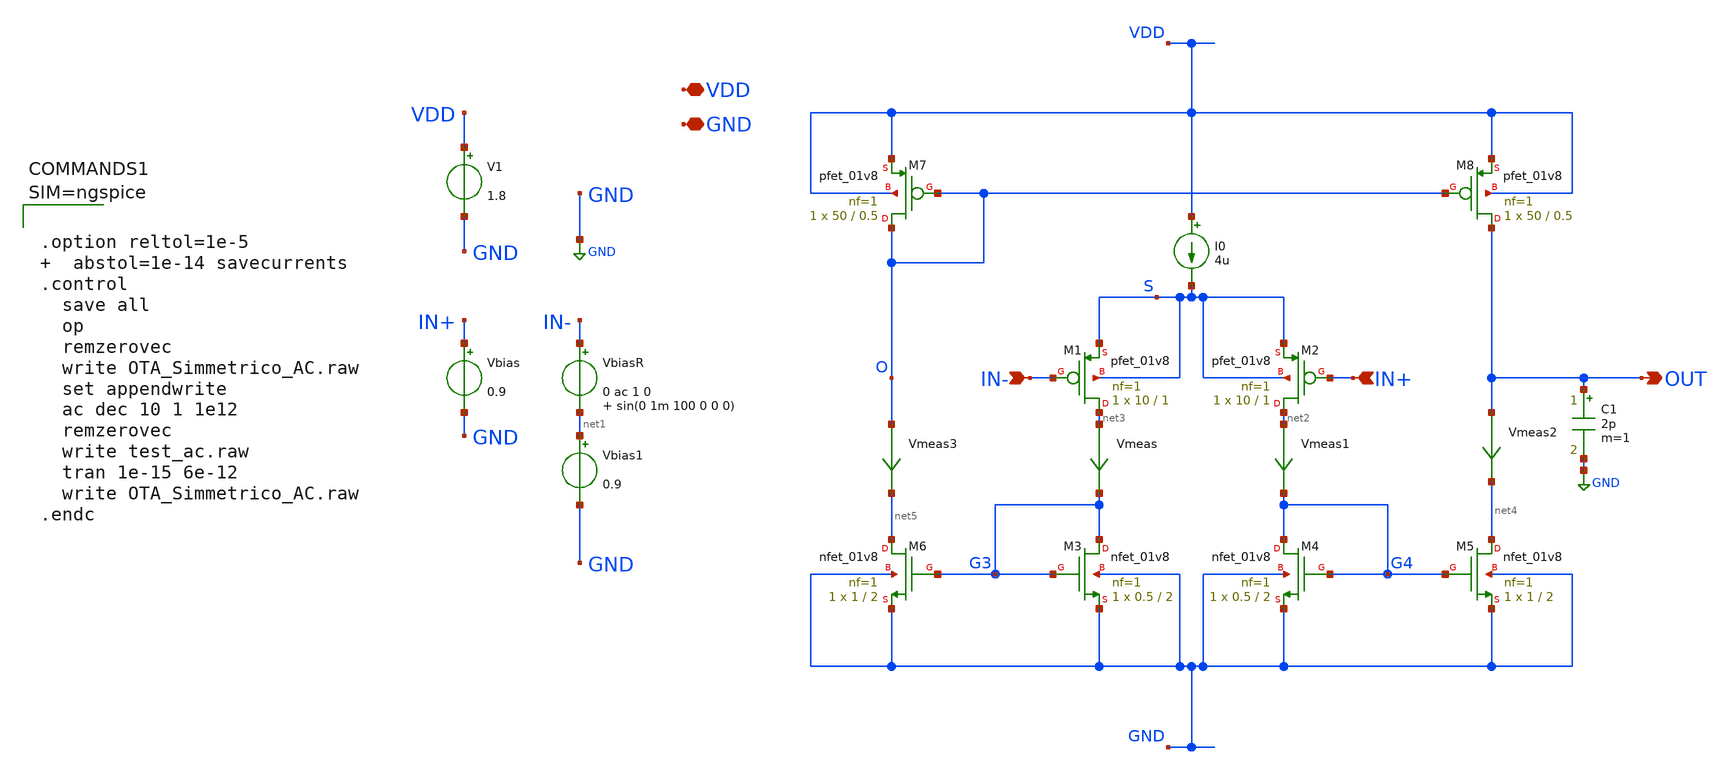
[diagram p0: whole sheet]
** sch_path: xschem/OTA_Simmetrico_AC.sch
**.subckt OTA_Simmetrico_AC VDD GND IN+ IN- OUT
*.iopin VDD
*.iopin GND
*.ipin IN+
*.ipin IN-
*.opin OUT
XM1 net3 IN- S S sky130_fd_pr__pfet_01v8 L=1 W=10 nf=1 ad='int((nf+1)/2) * W/nf * 0.29' as='int((nf+2)/2) * W/nf * 0.29'
+ pd='2*int((nf+1)/2) * (W/nf + 0.29)' ps='2*int((nf+2)/2) * (W/nf + 0.29)' nrd='0.29 / W' nrs='0.29 / W'
+ sa=0 sb=0 sd=0 mult=1 m=1
XM2 net2 IN+ S S sky130_fd_pr__pfet_01v8 L=1 W=10 nf=1 ad='int((nf+1)/2) * W/nf * 0.29' as='int((nf+2)/2) * W/nf * 0.29'
+ pd='2*int((nf+1)/2) * (W/nf + 0.29)' ps='2*int((nf+2)/2) * (W/nf + 0.29)' nrd='0.29 / W' nrs='0.29 / W'
+ sa=0 sb=0 sd=0 mult=1 m=1
XM3 G3 G3 GND GND sky130_fd_pr__nfet_01v8 L=2 W=0.5 nf=1 ad='int((nf+1)/2) * W/nf * 0.29' as='int((nf+2)/2) * W/nf * 0.29'
+ pd='2*int((nf+1)/2) * (W/nf + 0.29)' ps='2*int((nf+2)/2) * (W/nf + 0.29)' nrd='0.29 / W' nrs='0.29 / W'
+ sa=0 sb=0 sd=0 mult=1 m=1
XM4 G4 G4 GND GND sky130_fd_pr__nfet_01v8 L=2 W=0.5 nf=1 ad='int((nf+1)/2) * W/nf * 0.29' as='int((nf+2)/2) * W/nf * 0.29'
+ pd='2*int((nf+1)/2) * (W/nf + 0.29)' ps='2*int((nf+2)/2) * (W/nf + 0.29)' nrd='0.29 / W' nrs='0.29 / W'
+ sa=0 sb=0 sd=0 mult=1 m=1
XM5 net4 G4 GND GND sky130_fd_pr__nfet_01v8 L=2 W=1 nf=1 ad='int((nf+1)/2) * W/nf * 0.29' as='int((nf+2)/2) * W/nf * 0.29'
+ pd='2*int((nf+1)/2) * (W/nf + 0.29)' ps='2*int((nf+2)/2) * (W/nf + 0.29)' nrd='0.29 / W' nrs='0.29 / W'
+ sa=0 sb=0 sd=0 mult=1 m=1
XM6 net5 G3 GND GND sky130_fd_pr__nfet_01v8 L=2 W=1 nf=1 ad='int((nf+1)/2) * W/nf * 0.29' as='int((nf+2)/2) * W/nf * 0.29'
+ pd='2*int((nf+1)/2) * (W/nf + 0.29)' ps='2*int((nf+2)/2) * (W/nf + 0.29)' nrd='0.29 / W' nrs='0.29 / W'
+ sa=0 sb=0 sd=0 mult=1 m=1
XM7 O O VDD VDD sky130_fd_pr__pfet_01v8 L=0.5 W=50 nf=1 ad='int((nf+1)/2) * W/nf * 0.29' as='int((nf+2)/2) * W/nf * 0.29'
+ pd='2*int((nf+1)/2) * (W/nf + 0.29)' ps='2*int((nf+2)/2) * (W/nf + 0.29)' nrd='0.29 / W' nrs='0.29 / W'
+ sa=0 sb=0 sd=0 mult=1 m=1
XM8 OUT O VDD VDD sky130_fd_pr__pfet_01v8 L=0.5 W=50 nf=1 ad='int((nf+1)/2) * W/nf * 0.29' as='int((nf+2)/2) * W/nf * 0.29'
+ pd='2*int((nf+1)/2) * (W/nf + 0.29)' ps='2*int((nf+2)/2) * (W/nf + 0.29)' nrd='0.29 / W' nrs='0.29 / W'
+ sa=0 sb=0 sd=0 mult=1 m=1
I0 VDD S 4u
V1 VDD GND 1.8
Vbias IN+ GND 0.9
VbiasR IN- net1 0 ac 1 0 sin(0 1m 100 0 0 0)
Vmeas net3 G3 0
.save i(vmeas)
Vmeas1 net2 G4 0
.save i(vmeas1)
Vmeas2 OUT net4 0
.save i(vmeas2)
Vmeas3 O net5 0
.save i(vmeas3)
C1 OUT GND 2p m=1
Vbias1 net1 GND 0.9
**** begin user architecture code
.lib $::SKYWATER_MODELS/sky130.lib.spice tt



.option reltol=1e-5   abstol=1e-14 savecurrents
.control
  save all
  op
  remzerovec
  write OTA_Simmetrico_AC.raw
  set appendwrite
  ac dec 10 1 1e12
  remzerovec
  write test_ac.raw
  tran 1e-15 6e-12
  write OTA_Simmetrico_AC.raw
.endc



**** end user architecture code
**.ends
.GLOBAL GND
.end
